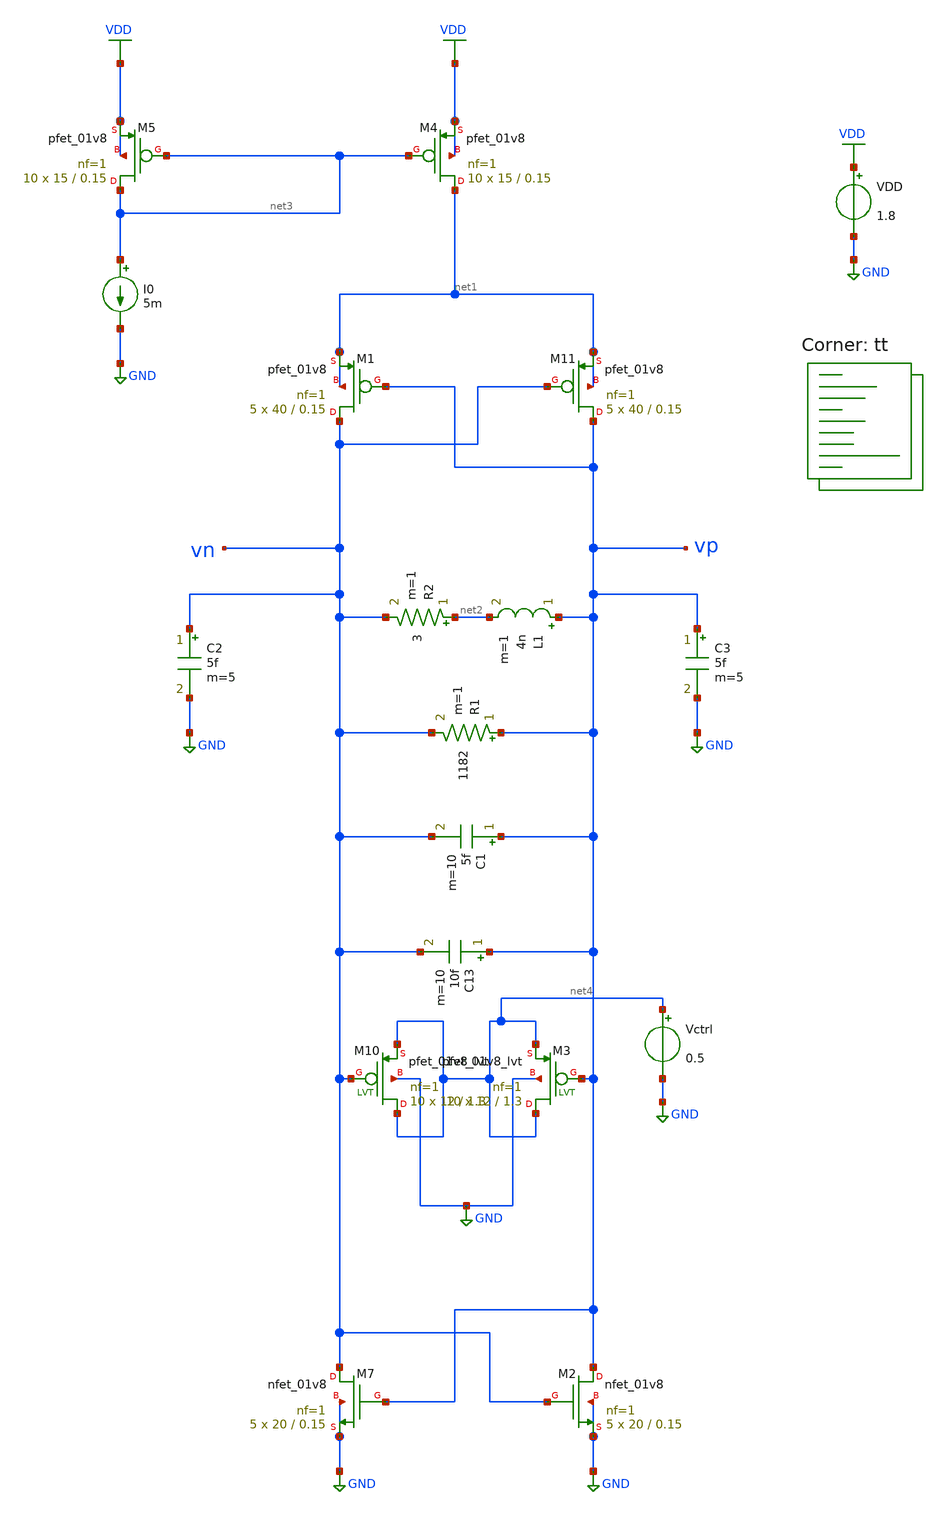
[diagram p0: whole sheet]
** sch_path: pll/lc_vco_lib/Ahmed_Reda/CMOS_LC_VCO_tb/xschem/CMOS_LC_VCO_tb.sch
**.subckt CMOS_LC_VCO_tb
XM11 vp vn net1 net1 sky130_fd_pr__pfet_01v8 L=0.15 W=40 nf=1 ad='int((nf+1)/2) * W/nf * 0.29' as='int((nf+2)/2) * W/nf * 0.29'
+ pd='2*int((nf+1)/2) * (W/nf + 0.29)' ps='2*int((nf+2)/2) * (W/nf + 0.29)' nrd='0.29 / W' nrs='0.29 / W'
+ sa=0 sb=0 sd=0 mult=5 m=5
XM1 vn vp net1 net1 sky130_fd_pr__pfet_01v8 L=0.15 W=40 nf=1 ad='int((nf+1)/2) * W/nf * 0.29' as='int((nf+2)/2) * W/nf * 0.29'
+ pd='2*int((nf+1)/2) * (W/nf + 0.29)' ps='2*int((nf+2)/2) * (W/nf + 0.29)' nrd='0.29 / W' nrs='0.29 / W'
+ sa=0 sb=0 sd=0 mult=5 m=5
XM2 vp vn GND GND sky130_fd_pr__nfet_01v8 L=0.15 W=20 nf=1 ad='int((1 + 1)/2) * 20 / 1 * 0.29' as='int((1 + 2)/2) * 20 / 1 * 0.29'
+ pd='2*int((1 + 1)/2) * (20 / 1 + 0.29)' ps='2*int((1 + 2)/2) * (20 / 1 + 0.29)' nrd='0.29 / 20 ' nrs='0.29 / 20 '
+ sa=0 sb=0 sd=0 mult=5 m=5
L1 vp net2 4n m=1
I0 net3 GND 5m
R1 vp vn 1182 m=1
VDD VDD GND 1.8
R2 net2 vn 3 m=1
XM4 net1 net3 VDD VDD sky130_fd_pr__pfet_01v8 L=0.15 W=15 nf=1 ad='int((nf+1)/2) * W/nf * 0.29' as='int((nf+2)/2) * W/nf * 0.29'
+ pd='2*int((nf+1)/2) * (W/nf + 0.29)' ps='2*int((nf+2)/2) * (W/nf + 0.29)' nrd='0.29 / W' nrs='0.29 / W'
+ sa=0 sb=0 sd=0 mult=10 m=10
XM5 net3 net3 VDD VDD sky130_fd_pr__pfet_01v8 L=0.15 W=15 nf=1 ad='int((nf+1)/2) * W/nf * 0.29' as='int((nf+2)/2) * W/nf * 0.29'
+ pd='2*int((nf+1)/2) * (W/nf + 0.29)' ps='2*int((nf+2)/2) * (W/nf + 0.29)' nrd='0.29 / W' nrs='0.29 / W'
+ sa=0 sb=0 sd=0 mult=10 m=10
XM7 vn vp GND GND sky130_fd_pr__nfet_01v8 L=0.15 W=20 nf=1 ad='int((1 + 1)/2) * 20 / 1 * 0.29' as='int((1 + 2)/2) * 20 / 1 * 0.29'
+ pd='2*int((1 + 1)/2) * (20 / 1 + 0.29)' ps='2*int((1 + 2)/2) * (20 / 1 + 0.29)' nrd='0.29 / 20 ' nrs='0.29 / 20 '
+ sa=0 sb=0 sd=0 mult=5 m=5
C1 vp vn 5f m=10
C3 vp GND 5f m=5
C2 vn GND 5f m=5
Vctrl net4 GND 0.5
XM10 net4 vn net4 GND sky130_fd_pr__pfet_01v8_lvt L=1.3 W=12 nf=1 ad='int((1 + 1)/2) * 12 / 1 * 0.29'
+ as='int((1 + 2)/2) * 12 / 1 * 0.29' pd='2*int((1 + 1)/2) * (12 / 1 + 0.29)' ps='2*int((1 + 2)/2) * (12 / 1 + 0.29)'
+ nrd='0.29 / 12 ' nrs='0.29 / 12 ' sa=0 sb=0 sd=0 mult=10 m=10
XM3 net4 vp net4 GND sky130_fd_pr__pfet_01v8_lvt L=1.3 W=12 nf=1 ad='int((1 + 1)/2) * 12 / 1 * 0.29'
+ as='int((1 + 2)/2) * 12 / 1 * 0.29' pd='2*int((1 + 1)/2) * (12 / 1 + 0.29)' ps='2*int((1 + 2)/2) * (12 / 1 + 0.29)'
+ nrd='0.29 / 12 ' nrs='0.29 / 12 ' sa=0 sb=0 sd=0 mult=10 m=10
C13 vp vn 10f m=10
**** begin user architecture code
.lib $::SKYWATER_MODELS/sky130.lib.spice tt

.tran 0.01n 0.03u
.save all
.control
run
*plot v(voutp)
*plot v(voutn)
plot v(vp)-v(vn)
*plot @R3[i]
*plot @R4[i]
*print @m.xm5.msky130_fd_pr__pfet_01v8[id]
*print @m.xm4.msky130_fd_pr__pfet_01v8[id]
*print @m.xm1.msky130_fd_pr__pfet_01v8[gm]
*print @m.xm3.msky130_fd_pr__nfet_01v8[gm]
*print 2/(@m.xm1.msky130_fd_pr__pfet_01v8[gm])+2/(@m.xm7.msky130_fd_pr__nfet_01v8[gm])
*print 2/(@m.xm1.msky130_fd_pr__pfet_01v8[gm])+2/(@m.xm7.msky130_fd_pr__nfet_01v8[gm])-616
.endc
.measure tran tperiod TRIG par('(v(vp)-v(vn))') VAL=1 RISE=6 TARG par('(v(vp)-v(vn))') VAL=1 RISE=7


** opencircuitdesign pdks install
.lib $::SKYWATER_MODELS/sky130.lib.spice tt


**** end user architecture code
**.ends
.GLOBAL GND
.GLOBAL VDD
.end
